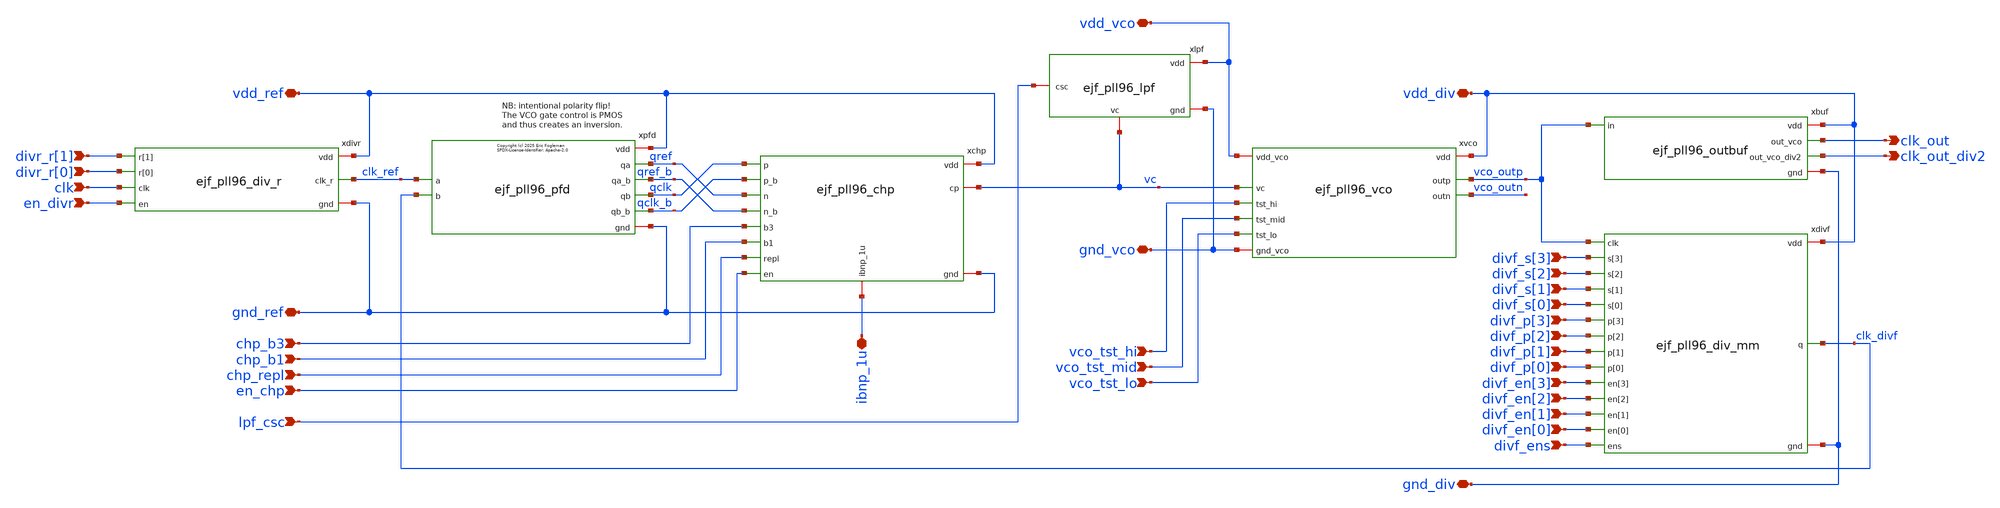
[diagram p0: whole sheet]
** sch_path: xschem/ejf_pll96.sch
**.subckt ejf_pll96 vdd_ref vdd_vco vdd_div gnd_ref ibnp_1u clk divf_s[3] divf_s[2] divf_s[1]
*+ divf_s[0] divf_p[3] divf_p[2] divf_p[1] divf_p[0] divf_en[3] divf_en[2] divf_en[1] divf_en[0] divf_ens
*+ clk_out clk_out_div2 gnd_vco gnd_div divr_r[1] divr_r[0] en_divr lpf_csc chp_b1 chp_b3 en_chp chp_repl
*+ vco_tst_hi vco_tst_mid vco_tst_lo
*.iopin vdd_ref
*.iopin vdd_vco
*.iopin vdd_div
*.iopin gnd_ref
*.iopin ibnp_1u
*.ipin clk
*.ipin divf_s[3]
*.ipin divf_s[2]
*.ipin divf_s[1]
*.ipin divf_s[0]
*.ipin divf_p[3]
*.ipin divf_p[2]
*.ipin divf_p[1]
*.ipin divf_p[0]
*.ipin divf_en[3]
*.ipin divf_en[2]
*.ipin divf_en[1]
*.ipin divf_en[0]
*.ipin divf_ens
*.opin clk_out
*.opin clk_out_div2
*.iopin gnd_vco
*.iopin gnd_div
*.ipin divr_r[1]
*.ipin divr_r[0]
*.ipin en_divr
*.ipin lpf_csc
*.ipin chp_b1
*.ipin chp_b3
*.ipin en_chp
*.ipin chp_repl
*.ipin vco_tst_hi
*.ipin vco_tst_mid
*.ipin vco_tst_lo
xlpf vdd_vco vc gnd_vco lpf_csc ejf_pll96_lpf
xpfd qref clk_ref qclk clk_divf vdd_ref gnd_ref qref_b qclk_b ejf_pll96_pfd
xchp vdd_ref qclk ibnp_1u qclk_b vc qref_b qref gnd_ref chp_b3 chp_b1 chp_repl en_chp ejf_pll96_chp
xvco vdd_vco vc vdd_div vco_outp vco_outn gnd_vco vco_tst_hi vco_tst_mid vco_tst_lo ejf_pll96_vco
xbuf vco_outp clk_out clk_out_div2 vdd_div gnd_div ejf_pll96_outbuf
xdivr en_divr clk clk_ref divr_r[0] divr_r[1] vdd_ref gnd_ref ejf_pll96_div_r
xdivf divf_p[3] vco_outp divf_p[2] divf_p[1] clk_divf divf_p[0] divf_en[3] divf_en[2] divf_en[1]
+ divf_s[3] divf_s[2] divf_s[1] divf_s[0] vdd_div gnd_div divf_en[0] divf_ens ejf_pll96_div_mm
**.ends
.end
